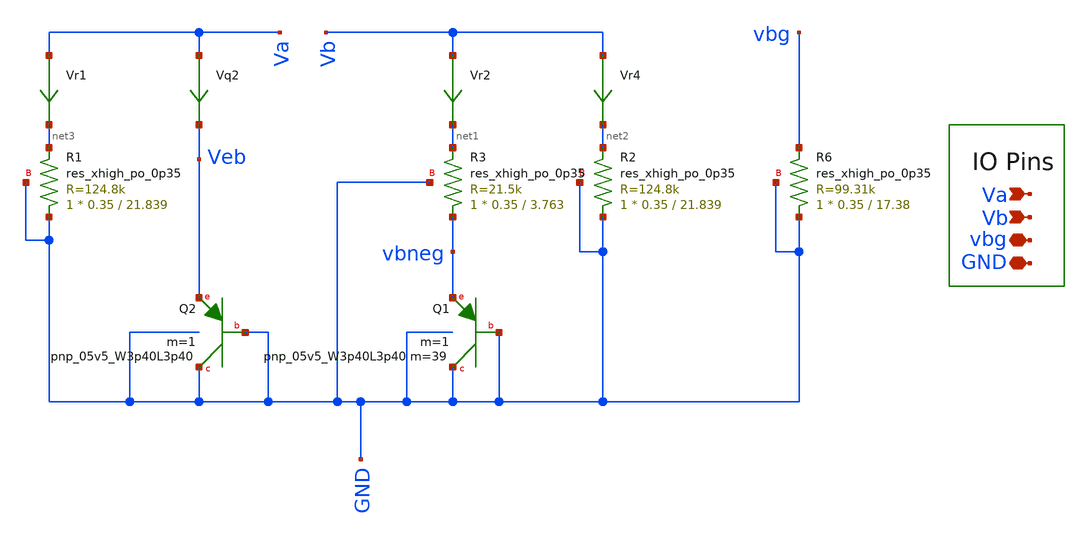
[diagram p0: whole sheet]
** sch_path: bandgap_sky130_v1/cascode_bandgapCore.sch
**.subckt cascode_bandgapCore Va Vb vbg GND
*.ipin Va
*.ipin Vb
*.iopin vbg
*.iopin GND
XQ2 GND GND Veb sky130_fd_pr__pnp_05v5_W3p40L3p40 m=1
Vr4 Vb net2 0
.save i(vr4)
Vr2 Vb net1 0
.save i(vr2)
Vr1 Va net3 0
.save i(vr1)
Vq2 Va Veb 0
.save i(vq2)
XQ1 GND GND vbneg sky130_fd_pr__pnp_05v5_W3p40L3p40 m=39 m=1
XR1 GND net3 GND sky130_fd_pr__res_xhigh_po_0p35 L=21.839 mult=1 m=1
XR2 GND net2 GND sky130_fd_pr__res_xhigh_po_0p35 L=21.839 mult=1 m=1
XR3 vbneg net1 GND sky130_fd_pr__res_xhigh_po_0p35 L=3.763 mult=1 m=1
XR6 GND vbg GND sky130_fd_pr__res_xhigh_po_0p35 L=17.38 mult=1 m=1
**.ends
.end
